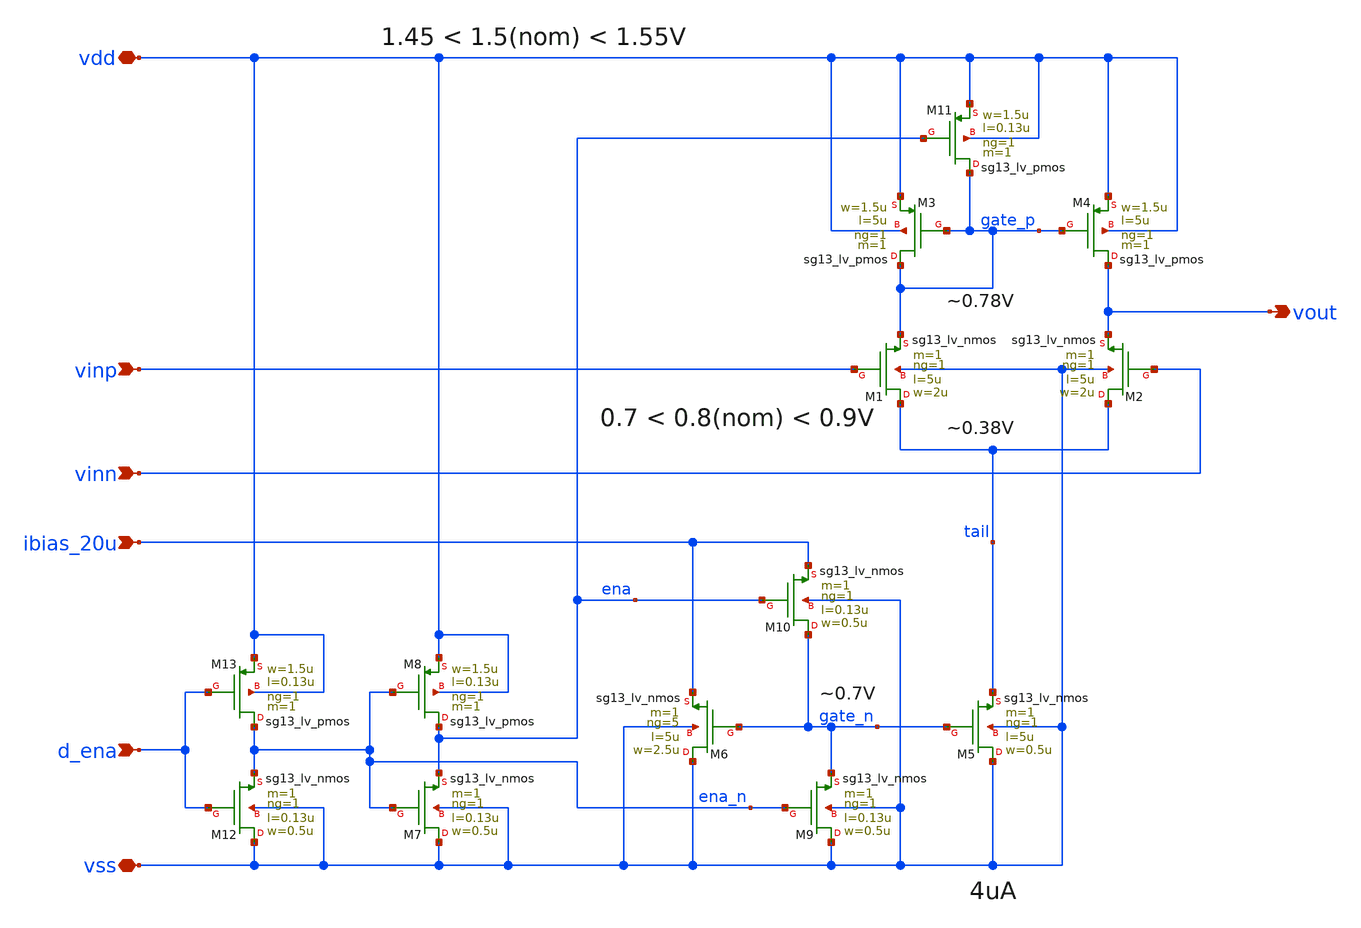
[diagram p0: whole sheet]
** sch_path: xschem/ota-5t.sch
* (c) 2024-2025 H. Pretl, Apache-2.0 license
**.subckt ota-5t ibias_20u vdd vss vinp vinn vout d_ena
*.ipin ibias_20u
*.iopin vdd
*.iopin vss
*.ipin vinp
*.ipin vinn
*.opin vout
*.ipin d_ena
XM5 vss gate_n tail vss sg13_lv_nmos w=0.5u l=5u ng=1 m=1 mm_ok=1
XM4 vout gate_p vdd vdd sg13_lv_pmos w=1.5u l=5u ng=1 m=1 mm_ok=1
XM1 tail vinp gate_p vss sg13_lv_nmos w=2u l=5u ng=1 m=1 mm_ok=1
XM2 tail vinn vout vss sg13_lv_nmos w=2u l=5u ng=1 m=1 mm_ok=1
XM3 gate_p gate_p vdd vdd sg13_lv_pmos w=1.5u l=5u ng=1 m=1 mm_ok=1
XM6 vss gate_n ibias_20u vss sg13_lv_nmos w=2.5u l=5u ng=5 m=1 mm_ok=1
XM9 vss ena_n gate_n vss sg13_lv_nmos w=0.5u l=0.13u ng=1 m=1 mm_ok=1
XM11 gate_p ena vdd vdd sg13_lv_pmos w=1.5u l=0.13u ng=1 m=1 mm_ok=1
XM7 vss ena_n ena vss sg13_lv_nmos w=0.5u l=0.13u ng=1 m=1 mm_ok=1
XM8 ena ena_n vdd vdd sg13_lv_pmos w=1.5u l=0.13u ng=1 m=1 mm_ok=1
XM10 gate_n ena ibias_20u vss sg13_lv_nmos w=0.5u l=0.13u ng=1 m=1 mm_ok=1
XM12 vss d_ena ena_n vss sg13_lv_nmos w=0.5u l=0.13u ng=1 m=1 mm_ok=1
XM13 ena_n d_ena vdd vdd sg13_lv_pmos w=1.5u l=0.13u ng=1 m=1 mm_ok=1
**.ends
.end
